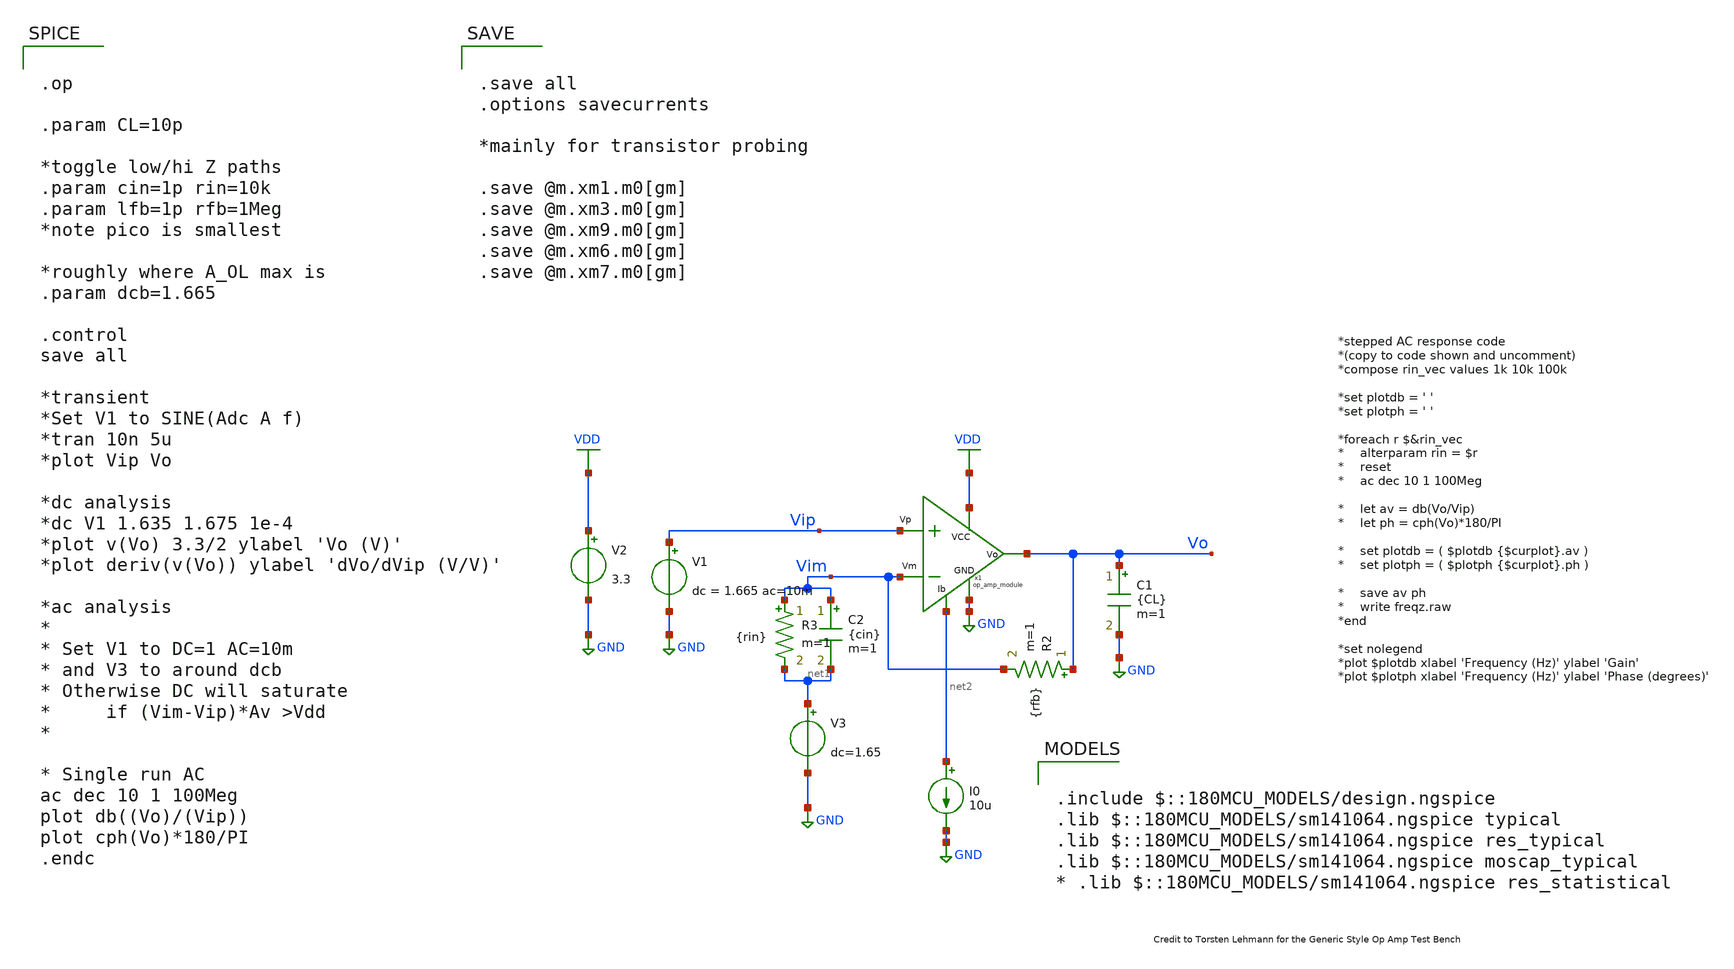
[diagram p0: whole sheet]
** sch_path: op_amp_tb.sch
**.subckt op_amp_tb
x1 VDD Vo Vip Vim net2 GND op_amp_module
V1 Vip GND dc = 1.665 ac=10m
V2 VDD GND 3.3
C1 Vo GND {CL} m=1
I0 net2 GND 10u
R2 Vo Vim {rfb} m=1
R3 Vim net1 {rin} m=1
V3 net1 GND dc=1.65
C2 Vim net1 {cin} m=1
**** begin user architecture code


.op

.param CL=10p

*toggle low/hi Z paths
.param cin=1p rin=10k
.param lfb=1p rfb=1Meg
*note pico is smallest

*roughly where A_OL max is
.param dcb=1.665

.control
save all

*transient
*Set V1 to SINE(Adc A f)
*tran 10n 5u
*plot Vip Vo

*dc analysis
*dc V1 1.635 1.675 1e-4
*plot v(Vo) 3.3/2 ylabel 'Vo (V)'
*plot deriv(v(Vo)) ylabel 'dVo/dVip (V/V)'

*ac analysis
*
* Set V1 to DC=1 AC=10m
* and V3 to around dcb
* Otherwise DC will saturate
* 	if (Vim-Vip)*Av >Vdd
*

* Single run AC
ac dec 10 1 100Meg
plot db((Vo)/(Vip))
plot cph(Vo)*180/PI
.endc




.save all
.options savecurrents

*mainly for transistor probing

.save @m.xm1.m0[gm]
.save @m.xm3.m0[gm]
.save @m.xm9.m0[gm]
.save @m.xm6.m0[gm]
.save @m.xm7.m0[gm]




.include $::180MCU_MODELS/design.ngspice
.lib $::180MCU_MODELS/sm141064.ngspice typical
.lib $::180MCU_MODELS/sm141064.ngspice res_typical
.lib $::180MCU_MODELS/sm141064.ngspice moscap_typical
* .lib $::180MCU_MODELS/sm141064.ngspice res_statistical

**** end user architecture code
**.ends

* expanding   symbol:  op_amp_module.sym # of pins=6
** sym_path: op_amp_module.sym
** sch_path: op_amp_module.sch
.subckt op_amp_module Vcc Vo Vp Vm Ib GND
*.ipin Vm
*.ipin Vp
*.ipin Vcc
*.ipin GND
*.opin Ib
*.opin Vo
XM4 net3 net3 net4 GND nfet_03v3 L=0.3u W=6.25u nf=1 ad='int((nf+1)/2) * W/nf * 0.18u' as='int((nf+2)/2) * W/nf * 0.18u'
+ pd='2*int((nf+1)/2) * (W/nf + 0.18u)' ps='2*int((nf+2)/2) * (W/nf + 0.18u)' nrd='0.18u / W' nrs='0.18u / W'
+ sa=0 sb=0 sd=0 m=1 par=1
XM2 net3 Vm net1 Vcc pfet_03v3 L=0.3u W=5.5u nf=1 ad='int((nf+1)/2) * W/nf * 0.18u' as='int((nf+2)/2) * W/nf * 0.18u'
+ pd='2*int((nf+1)/2) * (W/nf + 0.18u)' ps='2*int((nf+2)/2) * (W/nf + 0.18u)' nrd='0.18u / W' nrs='0.18u / W'
+ sa=0 sb=0 sd=0 m=1 par=1
XM3 net2 net3 net5 GND nfet_03v3 L=0.3u W=6.25u nf=1 ad='int((nf+1)/2) * W/nf * 0.18u' as='int((nf+2)/2) * W/nf * 0.18u'
+ pd='2*int((nf+1)/2) * (W/nf + 0.18u)' ps='2*int((nf+2)/2) * (W/nf + 0.18u)' nrd='0.18u / W' nrs='0.18u / W'
+ sa=0 sb=0 sd=0 m=1 par=1
XM1 net2 Vp net1 Vcc pfet_03v3 L=0.3u W=5.5u nf=1 ad='int((nf+1)/2) * W/nf * 0.18u' as='int((nf+2)/2) * W/nf * 0.18u'
+ pd='2*int((nf+1)/2) * (W/nf + 0.18u)' ps='2*int((nf+2)/2) * (W/nf + 0.18u)' nrd='0.18u / W' nrs='0.18u / W'
+ sa=0 sb=0 sd=0 m=1 par=1
XM5 net1 Ib Vcc Vcc pfet_03v3 L=0.3u W=24u nf=1 ad='int((nf+1)/2) * W/nf * 0.18u' as='int((nf+2)/2) * W/nf * 0.18u'
+ pd='2*int((nf+1)/2) * (W/nf + 0.18u)' ps='2*int((nf+2)/2) * (W/nf + 0.18u)' nrd='0.18u / W' nrs='0.18u / W'
+ sa=0 sb=0 sd=0 m=1 par=1
XM6 Vo Ib Vcc Vcc pfet_03v3 L=0.3u W=24u nf=1 ad='int((nf+1)/2) * W/nf * 0.18u' as='int((nf+2)/2) * W/nf * 0.18u'
+ pd='2*int((nf+1)/2) * (W/nf + 0.18u)' ps='2*int((nf+2)/2) * (W/nf + 0.18u)' nrd='0.18u / W' nrs='0.18u / W'
+ sa=0 sb=0 sd=0 m=1 par=1
XM8 Ib Ib Vcc Vcc pfet_03v3 L=0.3u W=24u nf=1 ad='int((nf+1)/2) * W/nf * 0.18u' as='int((nf+2)/2) * W/nf * 0.18u'
+ pd='2*int((nf+1)/2) * (W/nf + 0.18u)' ps='2*int((nf+2)/2) * (W/nf + 0.18u)' nrd='0.18u / W' nrs='0.18u / W'
+ sa=0 sb=0 sd=0 m=1 par=1
XM7 Vo net2 GND GND nfet_03v3 L=0.3u W=6.25u nf=1 ad='int((nf+1)/2) * W/nf * 0.18u' as='int((nf+2)/2) * W/nf * 0.18u'
+ pd='2*int((nf+1)/2) * (W/nf + 0.18u)' ps='2*int((nf+2)/2) * (W/nf + 0.18u)' nrd='0.18u / W' nrs='0.18u / W'
+ sa=0 sb=0 sd=0 m=1 par=1
XM10 net4 net4 GND GND nfet_03v3 L=0.3u W=6.25u nf=1 ad='int((nf+1)/2) * W/nf * 0.18u' as='int((nf+2)/2) * W/nf * 0.18u'
+ pd='2*int((nf+1)/2) * (W/nf + 0.18u)' ps='2*int((nf+2)/2) * (W/nf + 0.18u)' nrd='0.18u / W' nrs='0.18u / W'
+ sa=0 sb=0 sd=0 m=1 par=1
XM9 net5 net4 GND GND nfet_03v3 L=0.3u W=6.25u nf=1 ad='int((nf+1)/2) * W/nf * 0.18u' as='int((nf+2)/2) * W/nf * 0.18u'
+ pd='2*int((nf+1)/2) * (W/nf + 0.18u)' ps='2*int((nf+2)/2) * (W/nf + 0.18u)' nrd='0.18u / W' nrs='0.18u / W'
+ sa=0 sb=0 sd=0 m=1 par=1
XC2 net5 Vo cap_pmos_03v3 c_width=18u c_length=18u m=1
.ends

.GLOBAL GND
.GLOBAL VDD
.end
